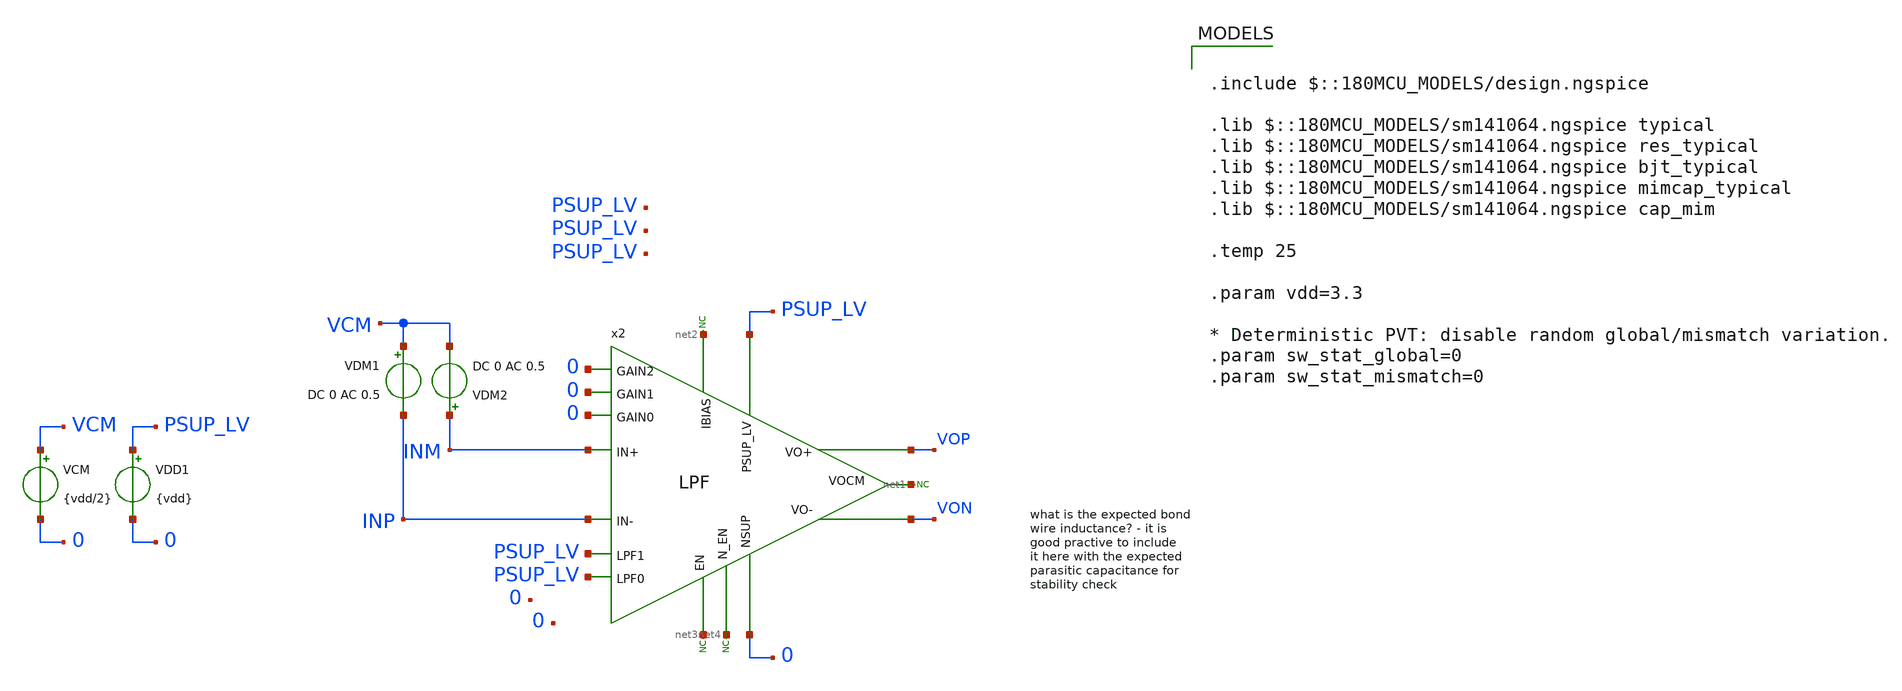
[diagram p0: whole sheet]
** sch_path: xschem/blocks/LPF/tb_LPF_gain.sch
**.subckt tb_LPF_gain
VDD1 PSUP_LV 0 {vdd}
VCM VCM 0 {vdd/2}
* noconn #net1
* noconn #net2
* noconn #net3
* noconn #net4
VDM2 INM VCM DC 0 AC 0.5
VDM1 VCM INP DC 0 AC 0.5
x2 PSUP_LV 0 net3 net4 net2 0 0 0 PSUP_LV PSUP_LV INM VOP net1 INP VON LPF
**** begin user architecture code

.include $::180MCU_MODELS/design.ngspice

.lib $::180MCU_MODELS/sm141064.ngspice typical
.lib $::180MCU_MODELS/sm141064.ngspice res_typical
.lib $::180MCU_MODELS/sm141064.ngspice bjt_typical
.lib $::180MCU_MODELS/sm141064.ngspice mimcap_typical
.lib $::180MCU_MODELS/sm141064.ngspice cap_mim

.temp 25

.param vdd=3.3

* Deterministic PVT: disable random global/mismatch variation.
.param sw_stat_global=0
.param sw_stat_mismatch=0



.control
set units=degrees
save all
ac dec 100 1 1G

let Vid = v(INP) - v(INM)
let Vo = v(Vop) - v(Von)
let aol = v(Vo) / v(Vid)
let gain_db = db(aol)
let phase_deg = cph(aol)

write tb_LPF_gain.raw frequency v(Vop) v(Von) v(Vo) aol gain_db phase_deg

.endc


**** end user architecture code
**.ends
.end
